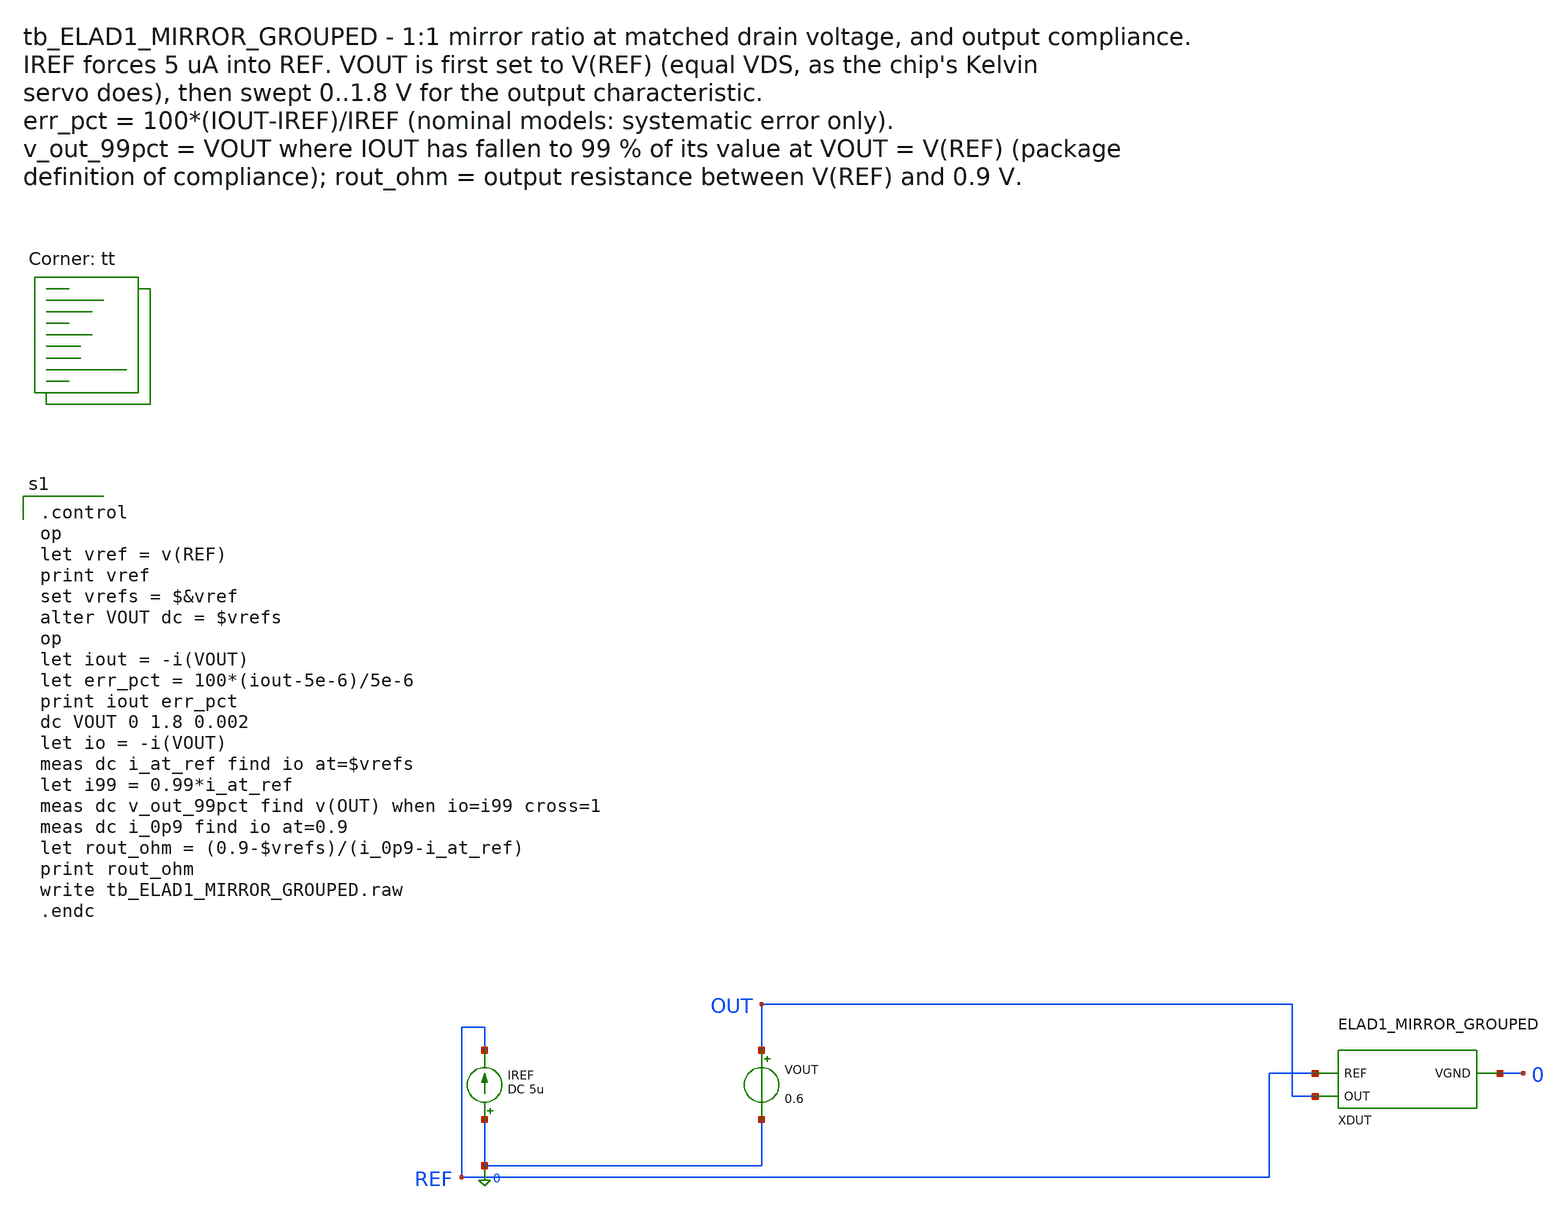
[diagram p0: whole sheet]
** sch_path: cells/ELAD1_MIRROR_GROUPED/schematic/tb_ELAD1_MIRROR_GROUPED.sch
**.subckt tb_ELAD1_MIRROR_GROUPED
IREF 0 REF DC 5u
VOUT OUT 0 0.6
XDUT REF OUT 0 ELAD1_MIRROR_GROUPED
**** begin user architecture code

.control
op
let vref = v(REF)
print vref
set vrefs = $&vref
alter VOUT dc = $vrefs
op
let iout = -i(VOUT)
let err_pct = 100*(iout-5e-6)/5e-6
print iout err_pct
dc VOUT 0 1.8 0.002
let io = -i(VOUT)
meas dc i_at_ref find io at=$vrefs
let i99 = 0.99*i_at_ref
meas dc v_out_99pct find v(OUT) when io=i99 cross=1
meas dc i_0p9 find io at=0.9
let rout_ohm = (0.9-$vrefs)/(i_0p9-i_at_ref)
print rout_ohm
write tb_ELAD1_MIRROR_GROUPED.raw
.endc

.lib $::SKYWATER_MODELS/sky130.lib.spice tt
**** end user architecture code
**.ends

* expanding   symbol:  ELAD1_MIRROR_GROUPED.sym # of pins=3
** sym_path: cells/ELAD1_MIRROR_GROUPED/schematic/ELAD1_MIRROR_GROUPED.sym
** sch_path: cells/ELAD1_MIRROR_GROUPED/schematic/ELAD1_MIRROR_GROUPED.sch
.subckt ELAD1_MIRROR_GROUPED REF OUT VGND
*.iopin REF
*.iopin OUT
*.iopin VGND
XA0 REF REF VGND VGND sky130_fd_pr__nfet_01v8 L=1 W=2 nf=1 ad='int((1 + 1)/2) * 2 / 1 * 0.29' as='int((1 + 2)/2) * 2 / 1 * 0.29'
+ pd='2*int((1 + 1)/2) * (2 / 1 + 0.29)' ps='2*int((1 + 2)/2) * (2 / 1 + 0.29)' nrd='0.29 / 2 ' nrs='0.29 / 2 '
+ sa=0 sb=0 sd=0 mult=1 m=1
XA1 REF REF VGND VGND sky130_fd_pr__nfet_01v8 L=1 W=2 nf=1 ad='int((1 + 1)/2) * 2 / 1 * 0.29' as='int((1 + 2)/2) * 2 / 1 * 0.29'
+ pd='2*int((1 + 1)/2) * (2 / 1 + 0.29)' ps='2*int((1 + 2)/2) * (2 / 1 + 0.29)' nrd='0.29 / 2 ' nrs='0.29 / 2 '
+ sa=0 sb=0 sd=0 mult=1 m=1
XA2 REF REF VGND VGND sky130_fd_pr__nfet_01v8 L=1 W=2 nf=1 ad='int((1 + 1)/2) * 2 / 1 * 0.29' as='int((1 + 2)/2) * 2 / 1 * 0.29'
+ pd='2*int((1 + 1)/2) * (2 / 1 + 0.29)' ps='2*int((1 + 2)/2) * (2 / 1 + 0.29)' nrd='0.29 / 2 ' nrs='0.29 / 2 '
+ sa=0 sb=0 sd=0 mult=1 m=1
XA3 REF REF VGND VGND sky130_fd_pr__nfet_01v8 L=1 W=2 nf=1 ad='int((1 + 1)/2) * 2 / 1 * 0.29' as='int((1 + 2)/2) * 2 / 1 * 0.29'
+ pd='2*int((1 + 1)/2) * (2 / 1 + 0.29)' ps='2*int((1 + 2)/2) * (2 / 1 + 0.29)' nrd='0.29 / 2 ' nrs='0.29 / 2 '
+ sa=0 sb=0 sd=0 mult=1 m=1
XB0 OUT REF VGND VGND sky130_fd_pr__nfet_01v8 L=1 W=2 nf=1 ad='int((1 + 1)/2) * 2 / 1 * 0.29' as='int((1 + 2)/2) * 2 / 1 * 0.29'
+ pd='2*int((1 + 1)/2) * (2 / 1 + 0.29)' ps='2*int((1 + 2)/2) * (2 / 1 + 0.29)' nrd='0.29 / 2 ' nrs='0.29 / 2 '
+ sa=0 sb=0 sd=0 mult=1 m=1
XB1 OUT REF VGND VGND sky130_fd_pr__nfet_01v8 L=1 W=2 nf=1 ad='int((1 + 1)/2) * 2 / 1 * 0.29' as='int((1 + 2)/2) * 2 / 1 * 0.29'
+ pd='2*int((1 + 1)/2) * (2 / 1 + 0.29)' ps='2*int((1 + 2)/2) * (2 / 1 + 0.29)' nrd='0.29 / 2 ' nrs='0.29 / 2 '
+ sa=0 sb=0 sd=0 mult=1 m=1
XB2 OUT REF VGND VGND sky130_fd_pr__nfet_01v8 L=1 W=2 nf=1 ad='int((1 + 1)/2) * 2 / 1 * 0.29' as='int((1 + 2)/2) * 2 / 1 * 0.29'
+ pd='2*int((1 + 1)/2) * (2 / 1 + 0.29)' ps='2*int((1 + 2)/2) * (2 / 1 + 0.29)' nrd='0.29 / 2 ' nrs='0.29 / 2 '
+ sa=0 sb=0 sd=0 mult=1 m=1
XB3 OUT REF VGND VGND sky130_fd_pr__nfet_01v8 L=1 W=2 nf=1 ad='int((1 + 1)/2) * 2 / 1 * 0.29' as='int((1 + 2)/2) * 2 / 1 * 0.29'
+ pd='2*int((1 + 1)/2) * (2 / 1 + 0.29)' ps='2*int((1 + 2)/2) * (2 / 1 + 0.29)' nrd='0.29 / 2 ' nrs='0.29 / 2 '
+ sa=0 sb=0 sd=0 mult=1 m=1
XDUM0 VGND VGND VGND VGND sky130_fd_pr__nfet_01v8 L=1 W=2 nf=1 ad='int((1 + 1)/2) * 2 / 1 * 0.29' as='int((1 + 2)/2) * 2 / 1 * 0.29'
+ pd='2*int((1 + 1)/2) * (2 / 1 + 0.29)' ps='2*int((1 + 2)/2) * (2 / 1 + 0.29)' nrd='0.29 / 2 ' nrs='0.29 / 2 '
+ sa=0 sb=0 sd=0 mult=1 m=1
XDUM1 VGND VGND VGND VGND sky130_fd_pr__nfet_01v8 L=1 W=2 nf=1 ad='int((1 + 1)/2) * 2 / 1 * 0.29' as='int((1 + 2)/2) * 2 / 1 * 0.29'
+ pd='2*int((1 + 1)/2) * (2 / 1 + 0.29)' ps='2*int((1 + 2)/2) * (2 / 1 + 0.29)' nrd='0.29 / 2 ' nrs='0.29 / 2 '
+ sa=0 sb=0 sd=0 mult=1 m=1
XDUM2 VGND VGND VGND VGND sky130_fd_pr__nfet_01v8 L=1 W=2 nf=1 ad='int((1 + 1)/2) * 2 / 1 * 0.29' as='int((1 + 2)/2) * 2 / 1 * 0.29'
+ pd='2*int((1 + 1)/2) * (2 / 1 + 0.29)' ps='2*int((1 + 2)/2) * (2 / 1 + 0.29)' nrd='0.29 / 2 ' nrs='0.29 / 2 '
+ sa=0 sb=0 sd=0 mult=1 m=1
XDUM3 VGND VGND VGND VGND sky130_fd_pr__nfet_01v8 L=1 W=2 nf=1 ad='int((1 + 1)/2) * 2 / 1 * 0.29' as='int((1 + 2)/2) * 2 / 1 * 0.29'
+ pd='2*int((1 + 1)/2) * (2 / 1 + 0.29)' ps='2*int((1 + 2)/2) * (2 / 1 + 0.29)' nrd='0.29 / 2 ' nrs='0.29 / 2 '
+ sa=0 sb=0 sd=0 mult=1 m=1
XDUM4 VGND VGND VGND VGND sky130_fd_pr__nfet_01v8 L=1 W=2 nf=1 ad='int((1 + 1)/2) * 2 / 1 * 0.29' as='int((1 + 2)/2) * 2 / 1 * 0.29'
+ pd='2*int((1 + 1)/2) * (2 / 1 + 0.29)' ps='2*int((1 + 2)/2) * (2 / 1 + 0.29)' nrd='0.29 / 2 ' nrs='0.29 / 2 '
+ sa=0 sb=0 sd=0 mult=1 m=1
XDUM5 VGND VGND VGND VGND sky130_fd_pr__nfet_01v8 L=1 W=2 nf=1 ad='int((1 + 1)/2) * 2 / 1 * 0.29' as='int((1 + 2)/2) * 2 / 1 * 0.29'
+ pd='2*int((1 + 1)/2) * (2 / 1 + 0.29)' ps='2*int((1 + 2)/2) * (2 / 1 + 0.29)' nrd='0.29 / 2 ' nrs='0.29 / 2 '
+ sa=0 sb=0 sd=0 mult=1 m=1
XDUM6 VGND VGND VGND VGND sky130_fd_pr__nfet_01v8 L=1 W=2 nf=1 ad='int((1 + 1)/2) * 2 / 1 * 0.29' as='int((1 + 2)/2) * 2 / 1 * 0.29'
+ pd='2*int((1 + 1)/2) * (2 / 1 + 0.29)' ps='2*int((1 + 2)/2) * (2 / 1 + 0.29)' nrd='0.29 / 2 ' nrs='0.29 / 2 '
+ sa=0 sb=0 sd=0 mult=1 m=1
XDUM7 VGND VGND VGND VGND sky130_fd_pr__nfet_01v8 L=1 W=2 nf=1 ad='int((1 + 1)/2) * 2 / 1 * 0.29' as='int((1 + 2)/2) * 2 / 1 * 0.29'
+ pd='2*int((1 + 1)/2) * (2 / 1 + 0.29)' ps='2*int((1 + 2)/2) * (2 / 1 + 0.29)' nrd='0.29 / 2 ' nrs='0.29 / 2 '
+ sa=0 sb=0 sd=0 mult=1 m=1
XDUM8 VGND VGND VGND VGND sky130_fd_pr__nfet_01v8 L=1 W=2 nf=1 ad='int((1 + 1)/2) * 2 / 1 * 0.29' as='int((1 + 2)/2) * 2 / 1 * 0.29'
+ pd='2*int((1 + 1)/2) * (2 / 1 + 0.29)' ps='2*int((1 + 2)/2) * (2 / 1 + 0.29)' nrd='0.29 / 2 ' nrs='0.29 / 2 '
+ sa=0 sb=0 sd=0 mult=1 m=1
XDUM9 VGND VGND VGND VGND sky130_fd_pr__nfet_01v8 L=1 W=2 nf=1 ad='int((1 + 1)/2) * 2 / 1 * 0.29' as='int((1 + 2)/2) * 2 / 1 * 0.29'
+ pd='2*int((1 + 1)/2) * (2 / 1 + 0.29)' ps='2*int((1 + 2)/2) * (2 / 1 + 0.29)' nrd='0.29 / 2 ' nrs='0.29 / 2 '
+ sa=0 sb=0 sd=0 mult=1 m=1
XDUM10 VGND VGND VGND VGND sky130_fd_pr__nfet_01v8 L=1 W=2 nf=1 ad='int((1 + 1)/2) * 2 / 1 * 0.29' as='int((1 + 2)/2) * 2 / 1 * 0.29'
+ pd='2*int((1 + 1)/2) * (2 / 1 + 0.29)' ps='2*int((1 + 2)/2) * (2 / 1 + 0.29)' nrd='0.29 / 2 ' nrs='0.29 / 2 '
+ sa=0 sb=0 sd=0 mult=1 m=1
XDUM11 VGND VGND VGND VGND sky130_fd_pr__nfet_01v8 L=1 W=2 nf=1 ad='int((1 + 1)/2) * 2 / 1 * 0.29' as='int((1 + 2)/2) * 2 / 1 * 0.29'
+ pd='2*int((1 + 1)/2) * (2 / 1 + 0.29)' ps='2*int((1 + 2)/2) * (2 / 1 + 0.29)' nrd='0.29 / 2 ' nrs='0.29 / 2 '
+ sa=0 sb=0 sd=0 mult=1 m=1
XDUM12 VGND VGND VGND VGND sky130_fd_pr__nfet_01v8 L=1 W=2 nf=1 ad='int((1 + 1)/2) * 2 / 1 * 0.29' as='int((1 + 2)/2) * 2 / 1 * 0.29'
+ pd='2*int((1 + 1)/2) * (2 / 1 + 0.29)' ps='2*int((1 + 2)/2) * (2 / 1 + 0.29)' nrd='0.29 / 2 ' nrs='0.29 / 2 '
+ sa=0 sb=0 sd=0 mult=1 m=1
XDUM13 VGND VGND VGND VGND sky130_fd_pr__nfet_01v8 L=1 W=2 nf=1 ad='int((1 + 1)/2) * 2 / 1 * 0.29' as='int((1 + 2)/2) * 2 / 1 * 0.29'
+ pd='2*int((1 + 1)/2) * (2 / 1 + 0.29)' ps='2*int((1 + 2)/2) * (2 / 1 + 0.29)' nrd='0.29 / 2 ' nrs='0.29 / 2 '
+ sa=0 sb=0 sd=0 mult=1 m=1
XDUM14 VGND VGND VGND VGND sky130_fd_pr__nfet_01v8 L=1 W=2 nf=1 ad='int((1 + 1)/2) * 2 / 1 * 0.29' as='int((1 + 2)/2) * 2 / 1 * 0.29'
+ pd='2*int((1 + 1)/2) * (2 / 1 + 0.29)' ps='2*int((1 + 2)/2) * (2 / 1 + 0.29)' nrd='0.29 / 2 ' nrs='0.29 / 2 '
+ sa=0 sb=0 sd=0 mult=1 m=1
XDUM15 VGND VGND VGND VGND sky130_fd_pr__nfet_01v8 L=1 W=2 nf=1 ad='int((1 + 1)/2) * 2 / 1 * 0.29' as='int((1 + 2)/2) * 2 / 1 * 0.29'
+ pd='2*int((1 + 1)/2) * (2 / 1 + 0.29)' ps='2*int((1 + 2)/2) * (2 / 1 + 0.29)' nrd='0.29 / 2 ' nrs='0.29 / 2 '
+ sa=0 sb=0 sd=0 mult=1 m=1
.ends

.end
